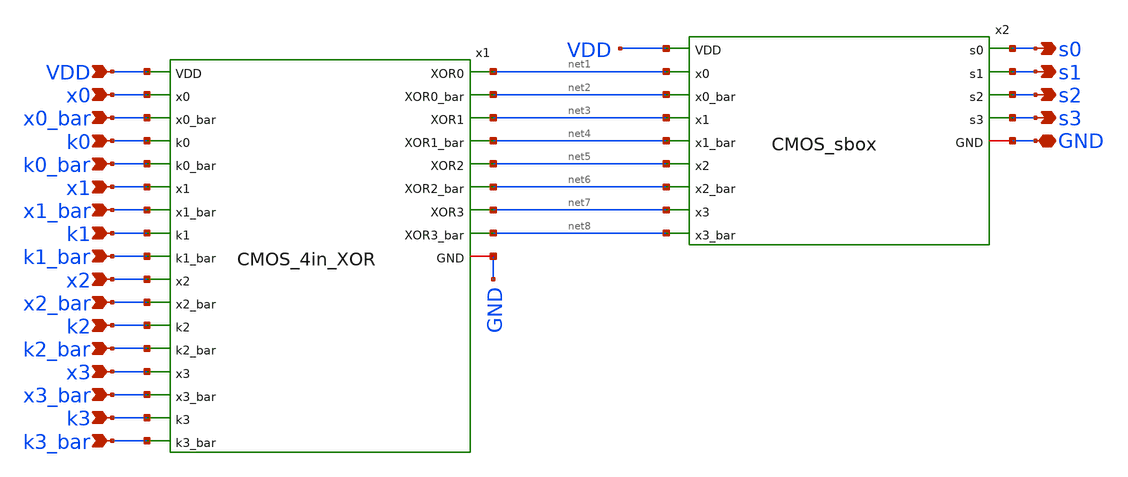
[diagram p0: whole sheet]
** sch_path: skywater_stuff/CMOS_PRESENT80_R1_lvs.sch
**.subckt CMOS_PRESENT80_R1_lvs GND x0 x0_bar k0 k0_bar x1 x1_bar k1 k1_bar x2 x2_bar k2 k2_bar x3
*+ x3_bar k3 k3_bar s0 s1 s2 s3 VDD
*.iopin GND
*.ipin x0
*.ipin x0_bar
*.ipin k0
*.ipin k0_bar
*.ipin x1
*.ipin x1_bar
*.ipin k1
*.ipin k1_bar
*.ipin x2
*.ipin x2_bar
*.ipin k2
*.ipin k2_bar
*.ipin x3
*.ipin x3_bar
*.ipin k3
*.ipin k3_bar
*.opin s0
*.opin s1
*.opin s2
*.opin s3
*.ipin VDD
x2 s0 VDD net1 net2 net3 net4 net5 net6 net7 net8 s1 s2 s3 GND CMOS_sbox
x1 VDD net1 x0 net2 x0_bar k0 k0_bar net3 x1 net4 x1_bar k1 k1_bar net5 x2 x2_bar net6 k2 k2_bar
+ net7 x3 GND net8 x3_bar k3 k3_bar CMOS_4in_XOR
**.ends
.end
